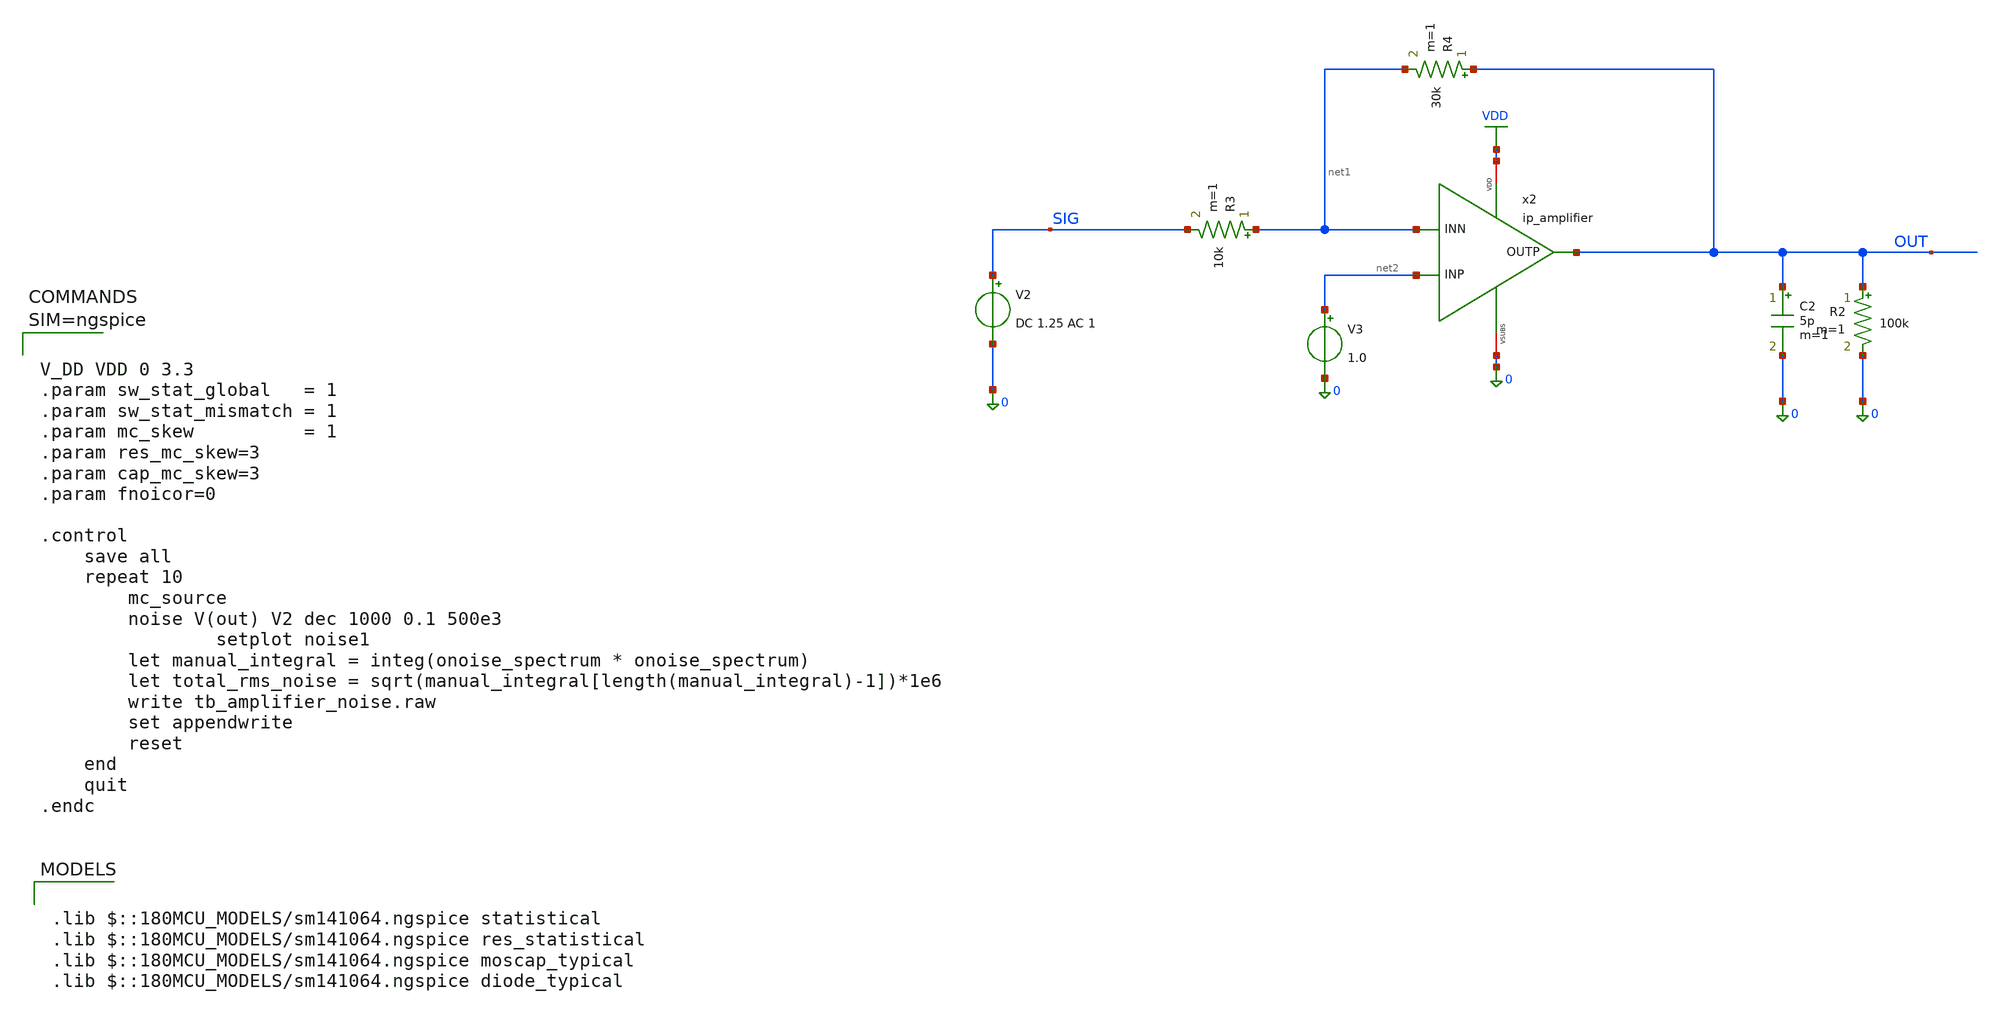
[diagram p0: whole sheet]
** sch_path: xschem/tb_amplifier_noise.sch
**.subckt tb_amplifier_noise
V2 SIG 0 DC 1.25 AC 1
x2 VDD OUT net2 net1 0 ip_amplifier
R2 OUT 0 100k m=1
C2 OUT 0 5p m=1
V3 net2 0 1.0
R3 net1 SIG 10k m=1
R4 OUT net1 30k m=1
**** begin user architecture code

.lib $::180MCU_MODELS/sm141064.ngspice statistical
.lib $::180MCU_MODELS/sm141064.ngspice res_statistical
.lib $::180MCU_MODELS/sm141064.ngspice moscap_typical
.lib $::180MCU_MODELS/sm141064.ngspice diode_typical




V_DD VDD 0 3.3
.param sw_stat_global   = 1
.param sw_stat_mismatch = 1
.param mc_skew          = 1
.param res_mc_skew=3
.param cap_mc_skew=3
.param fnoicor=0

.control
	save all
	repeat 10
		mc_source
		noise V(out) V2 dec 1000 0.1 500e3
                setplot noise1
		let manual_integral = integ(onoise_spectrum * onoise_spectrum)
		let total_rms_noise = sqrt(manual_integral[length(manual_integral)-1])*1e6
		write tb_amplifier_noise.raw
		set appendwrite
		reset
	end
	quit
.endc



**** end user architecture code
**.ends

* expanding   symbol:  ip_amplifier.sym # of pins=5
** sym_path: xschem/ip_amplifier.sym
** sch_path: xschem/ip_amplifier.sch
.subckt ip_amplifier VDD OUTP INP INN VSUBS
*.iopin VDD
*.iopin VSUBS
*.ipin INP
*.ipin INN
*.opin OUTP
XM1 net9 INP net7 VDD pfet_06v0 L=0.7u W=14u nf=1 ad='int((nf+1)/2) * W/nf * 0.18u' as='int((nf+2)/2) * W/nf * 0.18u'
+ pd='2*int((nf+1)/2) * (W/nf + 0.18u)' ps='2*int((nf+2)/2) * (W/nf + 0.18u)' nrd='0.18u / W' nrs='0.18u / W'
+ sa=0 sb=0 sd=0 m=1 par=1
XM2 net8 INN net7 VDD pfet_06v0 L=0.7u W=14u nf=1 ad='int((nf+1)/2) * W/nf * 0.18u' as='int((nf+2)/2) * W/nf * 0.18u'
+ pd='2*int((nf+1)/2) * (W/nf + 0.18u)' ps='2*int((nf+2)/2) * (W/nf + 0.18u)' nrd='0.18u / W' nrs='0.18u / W'
+ sa=0 sb=0 sd=0 m=1 par=1
XM5 net9 net1 VSUBS vsubs nfet_06v0 L=1u W=5u nf=1 ad='int((nf+1)/2) * W/nf * 0.18u' as='int((nf+2)/2) * W/nf * 0.18u'
+ pd='2*int((nf+1)/2) * (W/nf + 0.18u)' ps='2*int((nf+2)/2) * (W/nf + 0.18u)' nrd='0.18u / W' nrs='0.18u / W'
+ sa=0 sb=0 sd=0 m=1 par=1
XM6 net8 net1 VSUBS vsubs nfet_06v0 L=1u W=5u nf=1 ad='int((nf+1)/2) * W/nf * 0.18u' as='int((nf+2)/2) * W/nf * 0.18u'
+ pd='2*int((nf+1)/2) * (W/nf + 0.18u)' ps='2*int((nf+2)/2) * (W/nf + 0.18u)' nrd='0.18u / W' nrs='0.18u / W'
+ sa=0 sb=0 sd=0 m=1 par=1
XM3 net3 net1 VSUBS vsubs nfet_06v0 L=1u W=5u nf=1 ad='int((nf+1)/2) * W/nf * 0.18u' as='int((nf+2)/2) * W/nf * 0.18u'
+ pd='2*int((nf+1)/2) * (W/nf + 0.18u)' ps='2*int((nf+2)/2) * (W/nf + 0.18u)' nrd='0.18u / W' nrs='0.18u / W'
+ sa=0 sb=0 sd=0 m=1 par=1
XM4 net2 net1 VSUBS vsubs nfet_06v0 L=1u W=5u nf=1 ad='int((nf+1)/2) * W/nf * 0.18u' as='int((nf+2)/2) * W/nf * 0.18u'
+ pd='2*int((nf+1)/2) * (W/nf + 0.18u)' ps='2*int((nf+2)/2) * (W/nf + 0.18u)' nrd='0.18u / W' nrs='0.18u / W'
+ sa=0 sb=0 sd=0 m=1 par=1
XM7 net1 net1 net3 vsubs nfet_06v0 L=0.7u W=35u nf=1 ad='int((nf+1)/2) * W/nf * 0.18u' as='int((nf+2)/2) * W/nf * 0.18u'
+ pd='2*int((nf+1)/2) * (W/nf + 0.18u)' ps='2*int((nf+2)/2) * (W/nf + 0.18u)' nrd='0.18u / W' nrs='0.18u / W'
+ sa=0 sb=0 sd=0 m=1 par=1
XM8 net4 net1 net2 vsubs nfet_06v0 L=0.7u W=35u nf=1 ad='int((nf+1)/2) * W/nf * 0.18u' as='int((nf+2)/2) * W/nf * 0.18u'
+ pd='2*int((nf+1)/2) * (W/nf + 0.18u)' ps='2*int((nf+2)/2) * (W/nf + 0.18u)' nrd='0.18u / W' nrs='0.18u / W'
+ sa=0 sb=0 sd=0 m=1 par=1
I0 VDD net1 20u
XM9 net5 net4 VDD VDD pfet_06v0 L=1u W=6u nf=1 ad='int((nf+1)/2) * W/nf * 0.18u' as='int((nf+2)/2) * W/nf * 0.18u'
+ pd='2*int((nf+1)/2) * (W/nf + 0.18u)' ps='2*int((nf+2)/2) * (W/nf + 0.18u)' nrd='0.18u / W' nrs='0.18u / W'
+ sa=0 sb=0 sd=0 m=1 par=1
XM10 net6 net4 VDD VDD pfet_06v0 L=1u W=6u nf=1 ad='int((nf+1)/2) * W/nf * 0.18u' as='int((nf+2)/2) * W/nf * 0.18u'
+ pd='2*int((nf+1)/2) * (W/nf + 0.18u)' ps='2*int((nf+2)/2) * (W/nf + 0.18u)' nrd='0.18u / W' nrs='0.18u / W'
+ sa=0 sb=0 sd=0 m=1 par=1
XM11 net4 net4 net5 VDD pfet_06v0 L=0.7u W=35u nf=1 ad='int((nf+1)/2) * W/nf * 0.18u' as='int((nf+2)/2) * W/nf * 0.18u'
+ pd='2*int((nf+1)/2) * (W/nf + 0.18u)' ps='2*int((nf+2)/2) * (W/nf + 0.18u)' nrd='0.18u / W' nrs='0.18u / W'
+ sa=0 sb=0 sd=0 m=1 par=1
XM12 net7 net4 net6 VDD pfet_06v0 L=0.7u W=35u nf=1 ad='int((nf+1)/2) * W/nf * 0.18u' as='int((nf+2)/2) * W/nf * 0.18u'
+ pd='2*int((nf+1)/2) * (W/nf + 0.18u)' ps='2*int((nf+2)/2) * (W/nf + 0.18u)' nrd='0.18u / W' nrs='0.18u / W'
+ sa=0 sb=0 sd=0 m=1 par=1
XM13 net10 net1 net8 vsubs nfet_06v0 L=0.7u W=35u nf=1 ad='int((nf+1)/2) * W/nf * 0.18u' as='int((nf+2)/2) * W/nf * 0.18u'
+ pd='2*int((nf+1)/2) * (W/nf + 0.18u)' ps='2*int((nf+2)/2) * (W/nf + 0.18u)' nrd='0.18u / W' nrs='0.18u / W'
+ sa=0 sb=0 sd=0 m=1 par=1
XM14 net11 net1 net9 vsubs nfet_06v0 L=0.7u W=35u nf=1 ad='int((nf+1)/2) * W/nf * 0.18u' as='int((nf+2)/2) * W/nf * 0.18u'
+ pd='2*int((nf+1)/2) * (W/nf + 0.18u)' ps='2*int((nf+2)/2) * (W/nf + 0.18u)' nrd='0.18u / W' nrs='0.18u / W'
+ sa=0 sb=0 sd=0 m=1 par=1
XM15 net10 net10 VDD VDD pfet_06v0 L=0.7u W=14u nf=1 ad='int((nf+1)/2) * W/nf * 0.18u' as='int((nf+2)/2) * W/nf * 0.18u'
+ pd='2*int((nf+1)/2) * (W/nf + 0.18u)' ps='2*int((nf+2)/2) * (W/nf + 0.18u)' nrd='0.18u / W' nrs='0.18u / W'
+ sa=0 sb=0 sd=0 m=1 par=1
XM16 net11 net10 VDD VDD pfet_06v0 L=0.7u W=14u nf=1 ad='int((nf+1)/2) * W/nf * 0.18u' as='int((nf+2)/2) * W/nf * 0.18u'
+ pd='2*int((nf+1)/2) * (W/nf + 0.18u)' ps='2*int((nf+2)/2) * (W/nf + 0.18u)' nrd='0.18u / W' nrs='0.18u / W'
+ sa=0 sb=0 sd=0 m=1 par=1
XM17 OUTP net11 VDD VDD pfet_06v0 L=0.5u W=30u nf=1 ad='int((nf+1)/2) * W/nf * 0.18u' as='int((nf+2)/2) * W/nf * 0.18u'
+ pd='2*int((nf+1)/2) * (W/nf + 0.18u)' ps='2*int((nf+2)/2) * (W/nf + 0.18u)' nrd='0.18u / W' nrs='0.18u / W'
+ sa=0 sb=0 sd=0 m=1 par=1
XM18 OUTP net9 VSUBS vsubs nfet_06v0 L=5u W=10u nf=1 ad='int((nf+1)/2) * W/nf * 0.18u' as='int((nf+2)/2) * W/nf * 0.18u'
+ pd='2*int((nf+1)/2) * (W/nf + 0.18u)' ps='2*int((nf+2)/2) * (W/nf + 0.18u)' nrd='0.18u / W' nrs='0.18u / W'
+ sa=0 sb=0 sd=0 m=1 par=1
C1 OUTP net11 5p m=1
.ends

.GLOBAL VDD
.end
